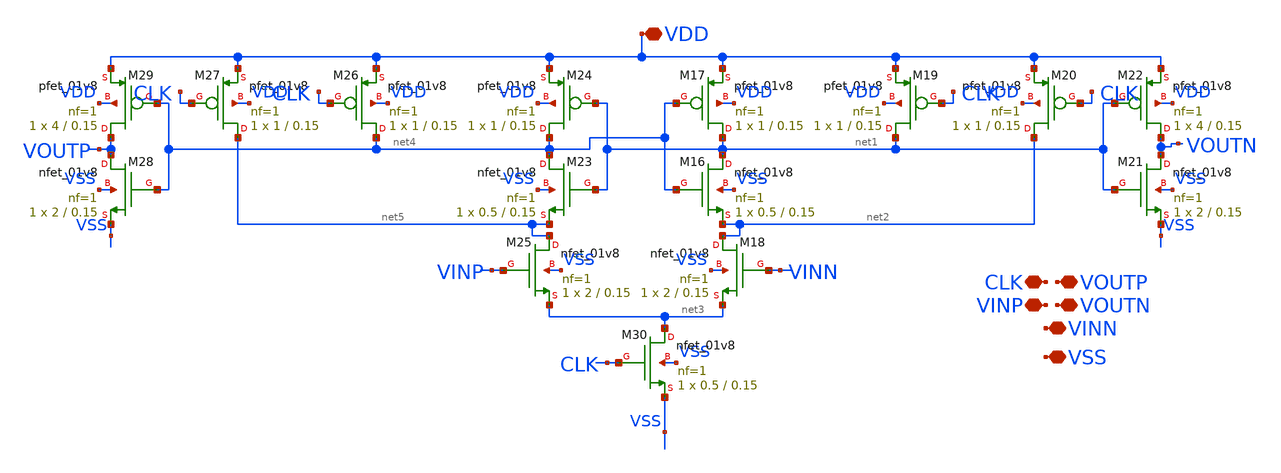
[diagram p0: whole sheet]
** sch_path: xschem/xschem_BGR_Top/Sigma_Delta/Comparator/Comparator.sch
**.subckt Comparator VDD VSS VOUTP VOUTN VINP VINN CLK
*.iopin VDD
*.iopin VSS
*.iopin VOUTP
*.iopin VOUTN
*.iopin VINP
*.iopin VINN
*.iopin CLK
XM16 net1 net4 net2 VSS sky130_fd_pr__nfet_01v8 L=0.15 W=0.5 nf=1 ad='int((nf+1)/2) * W/nf * 0.29' as='int((nf+2)/2) * W/nf * 0.29'
+ pd='2*int((nf+1)/2) * (W/nf + 0.29)' ps='2*int((nf+2)/2) * (W/nf + 0.29)' nrd='0.29 / W' nrs='0.29 / W'
+ sa=0 sb=0 sd=0 mult=1 m=1
XM17 net1 net4 VDD VDD sky130_fd_pr__pfet_01v8 L=0.15 W=1 nf=1 ad='int((nf+1)/2) * W/nf * 0.29' as='int((nf+2)/2) * W/nf * 0.29'
+ pd='2*int((nf+1)/2) * (W/nf + 0.29)' ps='2*int((nf+2)/2) * (W/nf + 0.29)' nrd='0.29 / W' nrs='0.29 / W'
+ sa=0 sb=0 sd=0 mult=1 m=1
XM18 net2 VINN net3 VSS sky130_fd_pr__nfet_01v8 L=0.15 W=2 nf=1 ad='int((nf+1)/2) * W/nf * 0.29' as='int((nf+2)/2) * W/nf * 0.29'
+ pd='2*int((nf+1)/2) * (W/nf + 0.29)' ps='2*int((nf+2)/2) * (W/nf + 0.29)' nrd='0.29 / W' nrs='0.29 / W'
+ sa=0 sb=0 sd=0 mult=1 m=1
XM19 net1 CLK VDD VDD sky130_fd_pr__pfet_01v8 L=0.15 W=1 nf=1 ad='int((nf+1)/2) * W/nf * 0.29' as='int((nf+2)/2) * W/nf * 0.29'
+ pd='2*int((nf+1)/2) * (W/nf + 0.29)' ps='2*int((nf+2)/2) * (W/nf + 0.29)' nrd='0.29 / W' nrs='0.29 / W'
+ sa=0 sb=0 sd=0 mult=1 m=1
XM20 net2 CLK VDD VDD sky130_fd_pr__pfet_01v8 L=0.15 W=1 nf=1 ad='int((nf+1)/2) * W/nf * 0.29' as='int((nf+2)/2) * W/nf * 0.29'
+ pd='2*int((nf+1)/2) * (W/nf + 0.29)' ps='2*int((nf+2)/2) * (W/nf + 0.29)' nrd='0.29 / W' nrs='0.29 / W'
+ sa=0 sb=0 sd=0 mult=1 m=1
XM21 VOUTN net1 VSS VSS sky130_fd_pr__nfet_01v8 L=0.15 W=2 nf=1 ad='int((nf+1)/2) * W/nf * 0.29' as='int((nf+2)/2) * W/nf * 0.29'
+ pd='2*int((nf+1)/2) * (W/nf + 0.29)' ps='2*int((nf+2)/2) * (W/nf + 0.29)' nrd='0.29 / W' nrs='0.29 / W'
+ sa=0 sb=0 sd=0 mult=1 m=1
XM22 VOUTN net1 VDD VDD sky130_fd_pr__pfet_01v8 L=0.15 W=4 nf=1 ad='int((nf+1)/2) * W/nf * 0.29' as='int((nf+2)/2) * W/nf * 0.29'
+ pd='2*int((nf+1)/2) * (W/nf + 0.29)' ps='2*int((nf+2)/2) * (W/nf + 0.29)' nrd='0.29 / W' nrs='0.29 / W'
+ sa=0 sb=0 sd=0 mult=1 m=1
XM23 net4 net1 net5 VSS sky130_fd_pr__nfet_01v8 L=0.15 W=0.5 nf=1 ad='int((nf+1)/2) * W/nf * 0.29' as='int((nf+2)/2) * W/nf * 0.29'
+ pd='2*int((nf+1)/2) * (W/nf + 0.29)' ps='2*int((nf+2)/2) * (W/nf + 0.29)' nrd='0.29 / W' nrs='0.29 / W'
+ sa=0 sb=0 sd=0 mult=1 m=1
XM24 net4 net1 VDD VDD sky130_fd_pr__pfet_01v8 L=0.15 W=1 nf=1 ad='int((nf+1)/2) * W/nf * 0.29' as='int((nf+2)/2) * W/nf * 0.29'
+ pd='2*int((nf+1)/2) * (W/nf + 0.29)' ps='2*int((nf+2)/2) * (W/nf + 0.29)' nrd='0.29 / W' nrs='0.29 / W'
+ sa=0 sb=0 sd=0 mult=1 m=1
XM25 net5 VINP net3 VSS sky130_fd_pr__nfet_01v8 L=0.15 W=2 nf=1 ad='int((nf+1)/2) * W/nf * 0.29' as='int((nf+2)/2) * W/nf * 0.29'
+ pd='2*int((nf+1)/2) * (W/nf + 0.29)' ps='2*int((nf+2)/2) * (W/nf + 0.29)' nrd='0.29 / W' nrs='0.29 / W'
+ sa=0 sb=0 sd=0 mult=1 m=1
XM26 net4 CLK VDD VDD sky130_fd_pr__pfet_01v8 L=0.15 W=1 nf=1 ad='int((nf+1)/2) * W/nf * 0.29' as='int((nf+2)/2) * W/nf * 0.29'
+ pd='2*int((nf+1)/2) * (W/nf + 0.29)' ps='2*int((nf+2)/2) * (W/nf + 0.29)' nrd='0.29 / W' nrs='0.29 / W'
+ sa=0 sb=0 sd=0 mult=1 m=1
XM27 net5 CLK VDD VDD sky130_fd_pr__pfet_01v8 L=0.15 W=1 nf=1 ad='int((nf+1)/2) * W/nf * 0.29' as='int((nf+2)/2) * W/nf * 0.29'
+ pd='2*int((nf+1)/2) * (W/nf + 0.29)' ps='2*int((nf+2)/2) * (W/nf + 0.29)' nrd='0.29 / W' nrs='0.29 / W'
+ sa=0 sb=0 sd=0 mult=1 m=1
XM28 VOUTP net4 VSS VSS sky130_fd_pr__nfet_01v8 L=0.15 W=2 nf=1 ad='int((nf+1)/2) * W/nf * 0.29' as='int((nf+2)/2) * W/nf * 0.29'
+ pd='2*int((nf+1)/2) * (W/nf + 0.29)' ps='2*int((nf+2)/2) * (W/nf + 0.29)' nrd='0.29 / W' nrs='0.29 / W'
+ sa=0 sb=0 sd=0 mult=1 m=1
XM29 VOUTP net4 VDD VDD sky130_fd_pr__pfet_01v8 L=0.15 W=4 nf=1 ad='int((nf+1)/2) * W/nf * 0.29' as='int((nf+2)/2) * W/nf * 0.29'
+ pd='2*int((nf+1)/2) * (W/nf + 0.29)' ps='2*int((nf+2)/2) * (W/nf + 0.29)' nrd='0.29 / W' nrs='0.29 / W'
+ sa=0 sb=0 sd=0 mult=1 m=1
XM30 net3 CLK VSS VSS sky130_fd_pr__nfet_01v8 L=0.15 W=0.5 nf=1 ad='int((nf+1)/2) * W/nf * 0.29' as='int((nf+2)/2) * W/nf * 0.29'
+ pd='2*int((nf+1)/2) * (W/nf + 0.29)' ps='2*int((nf+2)/2) * (W/nf + 0.29)' nrd='0.29 / W' nrs='0.29 / W'
+ sa=0 sb=0 sd=0 mult=1 m=1
**** begin user architecture code

** opencircuitdesign pdks install
.lib $::SKYWATER_MODELS/sky130.lib.spice tt


**** end user architecture code
**.ends
.end
